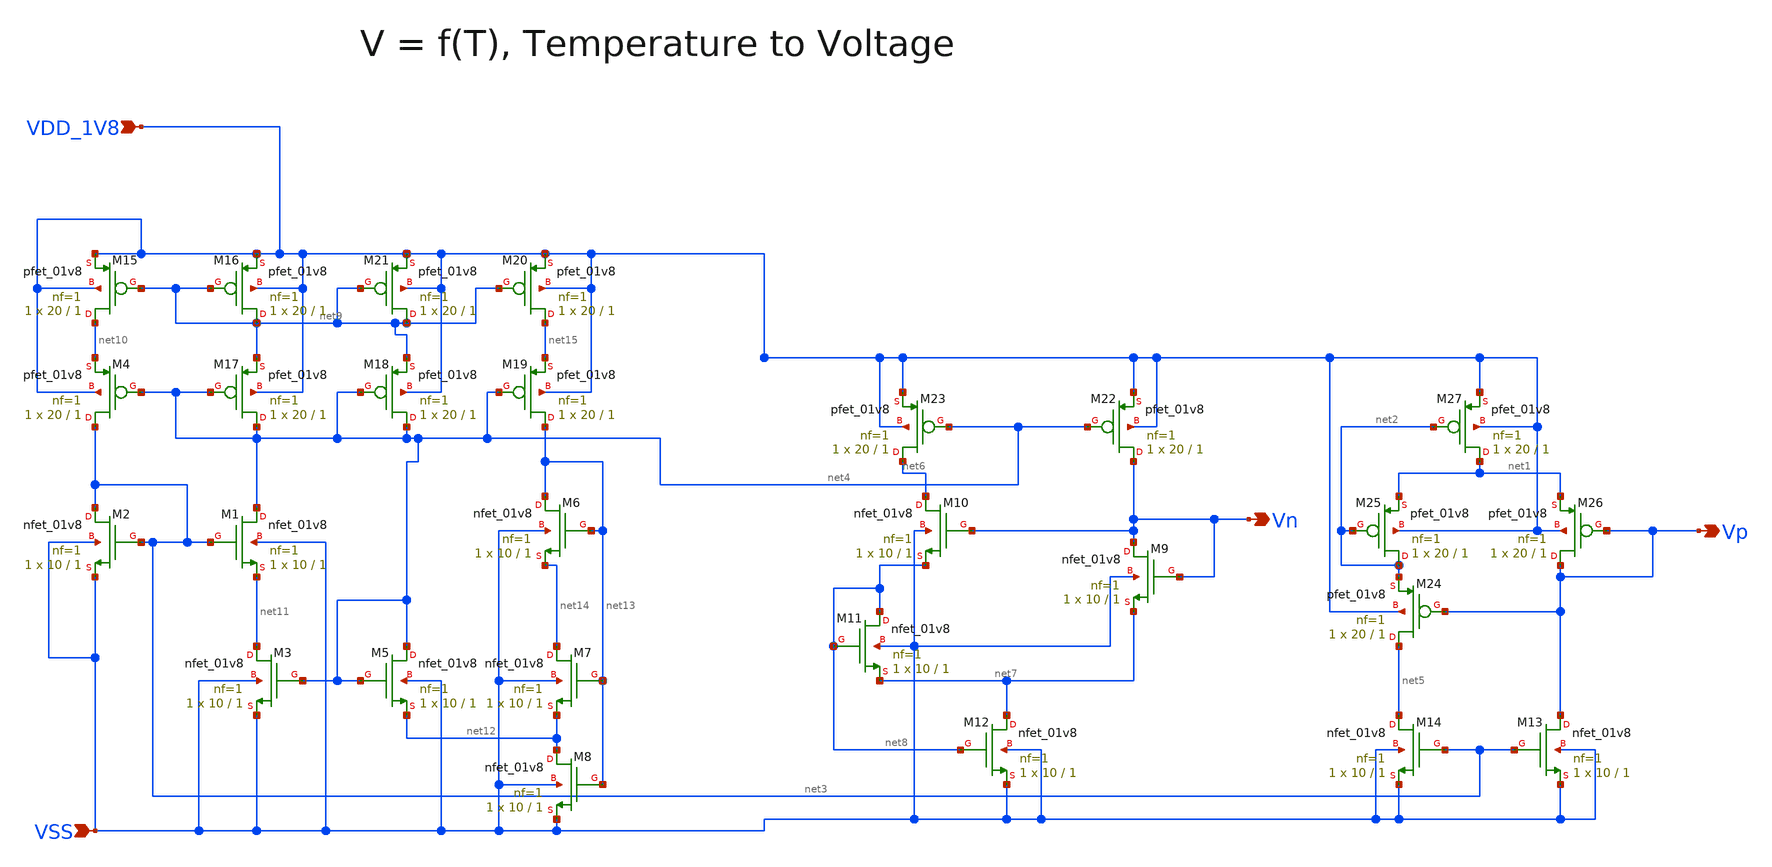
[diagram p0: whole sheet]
** sch_path: design/CNR_GR06_SKY130NM/CNR_GR06_test.sch
**.subckt CNR_GR06_test VDD_1V8 VSS Vn Vp
*.ipin VDD_1V8
*.ipin VSS
*.opin Vn
*.opin Vp
XM1 net4 net3 net11 VSS sky130_fd_pr__nfet_01v8 L=1 W=10 nf=1 ad='int((nf+1)/2) * W/nf * 0.29' as='int((nf+2)/2) * W/nf * 0.29'
+ pd='2*int((nf+1)/2) * (W/nf + 0.29)' ps='2*int((nf+2)/2) * (W/nf + 0.29)' nrd='0.29 / W' nrs='0.29 / W'
+ sa=0 sb=0 sd=0 mult=1 m=1
XM2 net3 net3 VSS VSS sky130_fd_pr__nfet_01v8 L=1 W=10 nf=1 ad='int((nf+1)/2) * W/nf * 0.29' as='int((nf+2)/2) * W/nf * 0.29'
+ pd='2*int((nf+1)/2) * (W/nf + 0.29)' ps='2*int((nf+2)/2) * (W/nf + 0.29)' nrd='0.29 / W' nrs='0.29 / W'
+ sa=0 sb=0 sd=0 mult=1 m=1
XM3 net11 net4 VSS VSS sky130_fd_pr__nfet_01v8 L=1 W=10 nf=1 ad='int((nf+1)/2) * W/nf * 0.29' as='int((nf+2)/2) * W/nf * 0.29'
+ pd='2*int((nf+1)/2) * (W/nf + 0.29)' ps='2*int((nf+2)/2) * (W/nf + 0.29)' nrd='0.29 / W' nrs='0.29 / W'
+ sa=0 sb=0 sd=0 mult=1 m=1
XM5 net4 net4 net12 VSS sky130_fd_pr__nfet_01v8 L=1 W=10 nf=1 ad='int((nf+1)/2) * W/nf * 0.29' as='int((nf+2)/2) * W/nf * 0.29'
+ pd='2*int((nf+1)/2) * (W/nf + 0.29)' ps='2*int((nf+2)/2) * (W/nf + 0.29)' nrd='0.29 / W' nrs='0.29 / W'
+ sa=0 sb=0 sd=0 mult=1 m=1
XM6 net13 net13 net14 VSS sky130_fd_pr__nfet_01v8 L=1 W=10 nf=1 ad='int((nf+1)/2) * W/nf * 0.29' as='int((nf+2)/2) * W/nf * 0.29'
+ pd='2*int((nf+1)/2) * (W/nf + 0.29)' ps='2*int((nf+2)/2) * (W/nf + 0.29)' nrd='0.29 / W' nrs='0.29 / W'
+ sa=0 sb=0 sd=0 mult=1 m=1
XM7 net14 net13 net12 VSS sky130_fd_pr__nfet_01v8 L=1 W=10 nf=1 ad='int((nf+1)/2) * W/nf * 0.29' as='int((nf+2)/2) * W/nf * 0.29'
+ pd='2*int((nf+1)/2) * (W/nf + 0.29)' ps='2*int((nf+2)/2) * (W/nf + 0.29)' nrd='0.29 / W' nrs='0.29 / W'
+ sa=0 sb=0 sd=0 mult=1 m=1
XM8 net12 net13 VSS VSS sky130_fd_pr__nfet_01v8 L=1 W=10 nf=1 ad='int((nf+1)/2) * W/nf * 0.29' as='int((nf+2)/2) * W/nf * 0.29'
+ pd='2*int((nf+1)/2) * (W/nf + 0.29)' ps='2*int((nf+2)/2) * (W/nf + 0.29)' nrd='0.29 / W' nrs='0.29 / W'
+ sa=0 sb=0 sd=0 mult=1 m=1
XM9 Vn Vn net7 VSS sky130_fd_pr__nfet_01v8 L=1 W=10 nf=1 ad='int((nf+1)/2) * W/nf * 0.29' as='int((nf+2)/2) * W/nf * 0.29'
+ pd='2*int((nf+1)/2) * (W/nf + 0.29)' ps='2*int((nf+2)/2) * (W/nf + 0.29)' nrd='0.29 / W' nrs='0.29 / W'
+ sa=0 sb=0 sd=0 mult=1 m=1
XM10 net6 Vn net8 VSS sky130_fd_pr__nfet_01v8 L=1 W=10 nf=1 ad='int((nf+1)/2) * W/nf * 0.29' as='int((nf+2)/2) * W/nf * 0.29'
+ pd='2*int((nf+1)/2) * (W/nf + 0.29)' ps='2*int((nf+2)/2) * (W/nf + 0.29)' nrd='0.29 / W' nrs='0.29 / W'
+ sa=0 sb=0 sd=0 mult=1 m=1
XM11 net8 net8 net7 VSS sky130_fd_pr__nfet_01v8 L=1 W=10 nf=1 ad='int((nf+1)/2) * W/nf * 0.29' as='int((nf+2)/2) * W/nf * 0.29'
+ pd='2*int((nf+1)/2) * (W/nf + 0.29)' ps='2*int((nf+2)/2) * (W/nf + 0.29)' nrd='0.29 / W' nrs='0.29 / W'
+ sa=0 sb=0 sd=0 mult=1 m=1
XM12 net7 net8 VSS VSS sky130_fd_pr__nfet_01v8 L=1 W=10 nf=1 ad='int((nf+1)/2) * W/nf * 0.29' as='int((nf+2)/2) * W/nf * 0.29'
+ pd='2*int((nf+1)/2) * (W/nf + 0.29)' ps='2*int((nf+2)/2) * (W/nf + 0.29)' nrd='0.29 / W' nrs='0.29 / W'
+ sa=0 sb=0 sd=0 mult=1 m=1
XM13 Vp net3 VSS VSS sky130_fd_pr__nfet_01v8 L=1 W=10 nf=1 ad='int((nf+1)/2) * W/nf * 0.29' as='int((nf+2)/2) * W/nf * 0.29'
+ pd='2*int((nf+1)/2) * (W/nf + 0.29)' ps='2*int((nf+2)/2) * (W/nf + 0.29)' nrd='0.29 / W' nrs='0.29 / W'
+ sa=0 sb=0 sd=0 mult=1 m=1
XM14 net5 net3 VSS VSS sky130_fd_pr__nfet_01v8 L=1 W=10 nf=1 ad='int((nf+1)/2) * W/nf * 0.29' as='int((nf+2)/2) * W/nf * 0.29'
+ pd='2*int((nf+1)/2) * (W/nf + 0.29)' ps='2*int((nf+2)/2) * (W/nf + 0.29)' nrd='0.29 / W' nrs='0.29 / W'
+ sa=0 sb=0 sd=0 mult=1 m=1
XM4 net3 net4 net10 VDD_1V8 sky130_fd_pr__pfet_01v8 L=1 W=20 nf=1 ad='int((nf+1)/2) * W/nf * 0.29' as='int((nf+2)/2) * W/nf * 0.29'
+ pd='2*int((nf+1)/2) * (W/nf + 0.29)' ps='2*int((nf+2)/2) * (W/nf + 0.29)' nrd='0.29 / W' nrs='0.29 / W'
+ sa=0 sb=0 sd=0 mult=1 m=1
XM15 net10 net9 VDD_1V8 VDD_1V8 sky130_fd_pr__pfet_01v8 L=1 W=20 nf=1 ad='int((nf+1)/2) * W/nf * 0.29'
+ as='int((nf+2)/2) * W/nf * 0.29' pd='2*int((nf+1)/2) * (W/nf + 0.29)' ps='2*int((nf+2)/2) * (W/nf + 0.29)'
+ nrd='0.29 / W' nrs='0.29 / W' sa=0 sb=0 sd=0 mult=1 m=1
XM16 net9 net9 VDD_1V8 VDD_1V8 sky130_fd_pr__pfet_01v8 L=1 W=20 nf=1 ad='int((nf+1)/2) * W/nf * 0.29'
+ as='int((nf+2)/2) * W/nf * 0.29' pd='2*int((nf+1)/2) * (W/nf + 0.29)' ps='2*int((nf+2)/2) * (W/nf + 0.29)'
+ nrd='0.29 / W' nrs='0.29 / W' sa=0 sb=0 sd=0 mult=1 m=1
XM17 net4 net4 net9 VDD_1V8 sky130_fd_pr__pfet_01v8 L=1 W=20 nf=1 ad='int((nf+1)/2) * W/nf * 0.29' as='int((nf+2)/2) * W/nf * 0.29'
+ pd='2*int((nf+1)/2) * (W/nf + 0.29)' ps='2*int((nf+2)/2) * (W/nf + 0.29)' nrd='0.29 / W' nrs='0.29 / W'
+ sa=0 sb=0 sd=0 mult=1 m=1
XM18 net4 net4 net9 VDD_1V8 sky130_fd_pr__pfet_01v8 L=1 W=20 nf=1 ad='int((nf+1)/2) * W/nf * 0.29' as='int((nf+2)/2) * W/nf * 0.29'
+ pd='2*int((nf+1)/2) * (W/nf + 0.29)' ps='2*int((nf+2)/2) * (W/nf + 0.29)' nrd='0.29 / W' nrs='0.29 / W'
+ sa=0 sb=0 sd=0 mult=1 m=1
XM19 net13 net4 net15 VDD_1V8 sky130_fd_pr__pfet_01v8 L=1 W=20 nf=1 ad='int((nf+1)/2) * W/nf * 0.29'
+ as='int((nf+2)/2) * W/nf * 0.29' pd='2*int((nf+1)/2) * (W/nf + 0.29)' ps='2*int((nf+2)/2) * (W/nf + 0.29)'
+ nrd='0.29 / W' nrs='0.29 / W' sa=0 sb=0 sd=0 mult=1 m=1
XM20 net15 net9 VDD_1V8 VDD_1V8 sky130_fd_pr__pfet_01v8 L=1 W=20 nf=1 ad='int((nf+1)/2) * W/nf * 0.29'
+ as='int((nf+2)/2) * W/nf * 0.29' pd='2*int((nf+1)/2) * (W/nf + 0.29)' ps='2*int((nf+2)/2) * (W/nf + 0.29)'
+ nrd='0.29 / W' nrs='0.29 / W' sa=0 sb=0 sd=0 mult=1 m=1
XM21 net9 net9 VDD_1V8 VDD_1V8 sky130_fd_pr__pfet_01v8 L=1 W=20 nf=1 ad='int((nf+1)/2) * W/nf * 0.29'
+ as='int((nf+2)/2) * W/nf * 0.29' pd='2*int((nf+1)/2) * (W/nf + 0.29)' ps='2*int((nf+2)/2) * (W/nf + 0.29)'
+ nrd='0.29 / W' nrs='0.29 / W' sa=0 sb=0 sd=0 mult=1 m=1
XM22 Vn net4 VDD_1V8 VDD_1V8 sky130_fd_pr__pfet_01v8 L=1 W=20 nf=1 ad='int((nf+1)/2) * W/nf * 0.29' as='int((nf+2)/2) * W/nf * 0.29'
+ pd='2*int((nf+1)/2) * (W/nf + 0.29)' ps='2*int((nf+2)/2) * (W/nf + 0.29)' nrd='0.29 / W' nrs='0.29 / W'
+ sa=0 sb=0 sd=0 mult=1 m=1
XM23 net6 net4 VDD_1V8 VDD_1V8 sky130_fd_pr__pfet_01v8 L=1 W=20 nf=1 ad='int((nf+1)/2) * W/nf * 0.29'
+ as='int((nf+2)/2) * W/nf * 0.29' pd='2*int((nf+1)/2) * (W/nf + 0.29)' ps='2*int((nf+2)/2) * (W/nf + 0.29)'
+ nrd='0.29 / W' nrs='0.29 / W' sa=0 sb=0 sd=0 mult=1 m=1
XM24 net5 Vp net2 VDD_1V8 sky130_fd_pr__pfet_01v8 L=1 W=20 nf=1 ad='int((nf+1)/2) * W/nf * 0.29' as='int((nf+2)/2) * W/nf * 0.29'
+ pd='2*int((nf+1)/2) * (W/nf + 0.29)' ps='2*int((nf+2)/2) * (W/nf + 0.29)' nrd='0.29 / W' nrs='0.29 / W'
+ sa=0 sb=0 sd=0 mult=1 m=1
XM25 net2 net2 net1 VDD_1V8 sky130_fd_pr__pfet_01v8 L=1 W=20 nf=1 ad='int((nf+1)/2) * W/nf * 0.29' as='int((nf+2)/2) * W/nf * 0.29'
+ pd='2*int((nf+1)/2) * (W/nf + 0.29)' ps='2*int((nf+2)/2) * (W/nf + 0.29)' nrd='0.29 / W' nrs='0.29 / W'
+ sa=0 sb=0 sd=0 mult=1 m=1
XM26 Vp Vp net1 VDD_1V8 sky130_fd_pr__pfet_01v8 L=1 W=20 nf=1 ad='int((nf+1)/2) * W/nf * 0.29' as='int((nf+2)/2) * W/nf * 0.29'
+ pd='2*int((nf+1)/2) * (W/nf + 0.29)' ps='2*int((nf+2)/2) * (W/nf + 0.29)' nrd='0.29 / W' nrs='0.29 / W'
+ sa=0 sb=0 sd=0 mult=1 m=1
XM27 net1 net2 VDD_1V8 VDD_1V8 sky130_fd_pr__pfet_01v8 L=1 W=20 nf=1 ad='int((nf+1)/2) * W/nf * 0.29'
+ as='int((nf+2)/2) * W/nf * 0.29' pd='2*int((nf+1)/2) * (W/nf + 0.29)' ps='2*int((nf+2)/2) * (W/nf + 0.29)'
+ nrd='0.29 / W' nrs='0.29 / W' sa=0 sb=0 sd=0 mult=1 m=1
**.ends
.end
